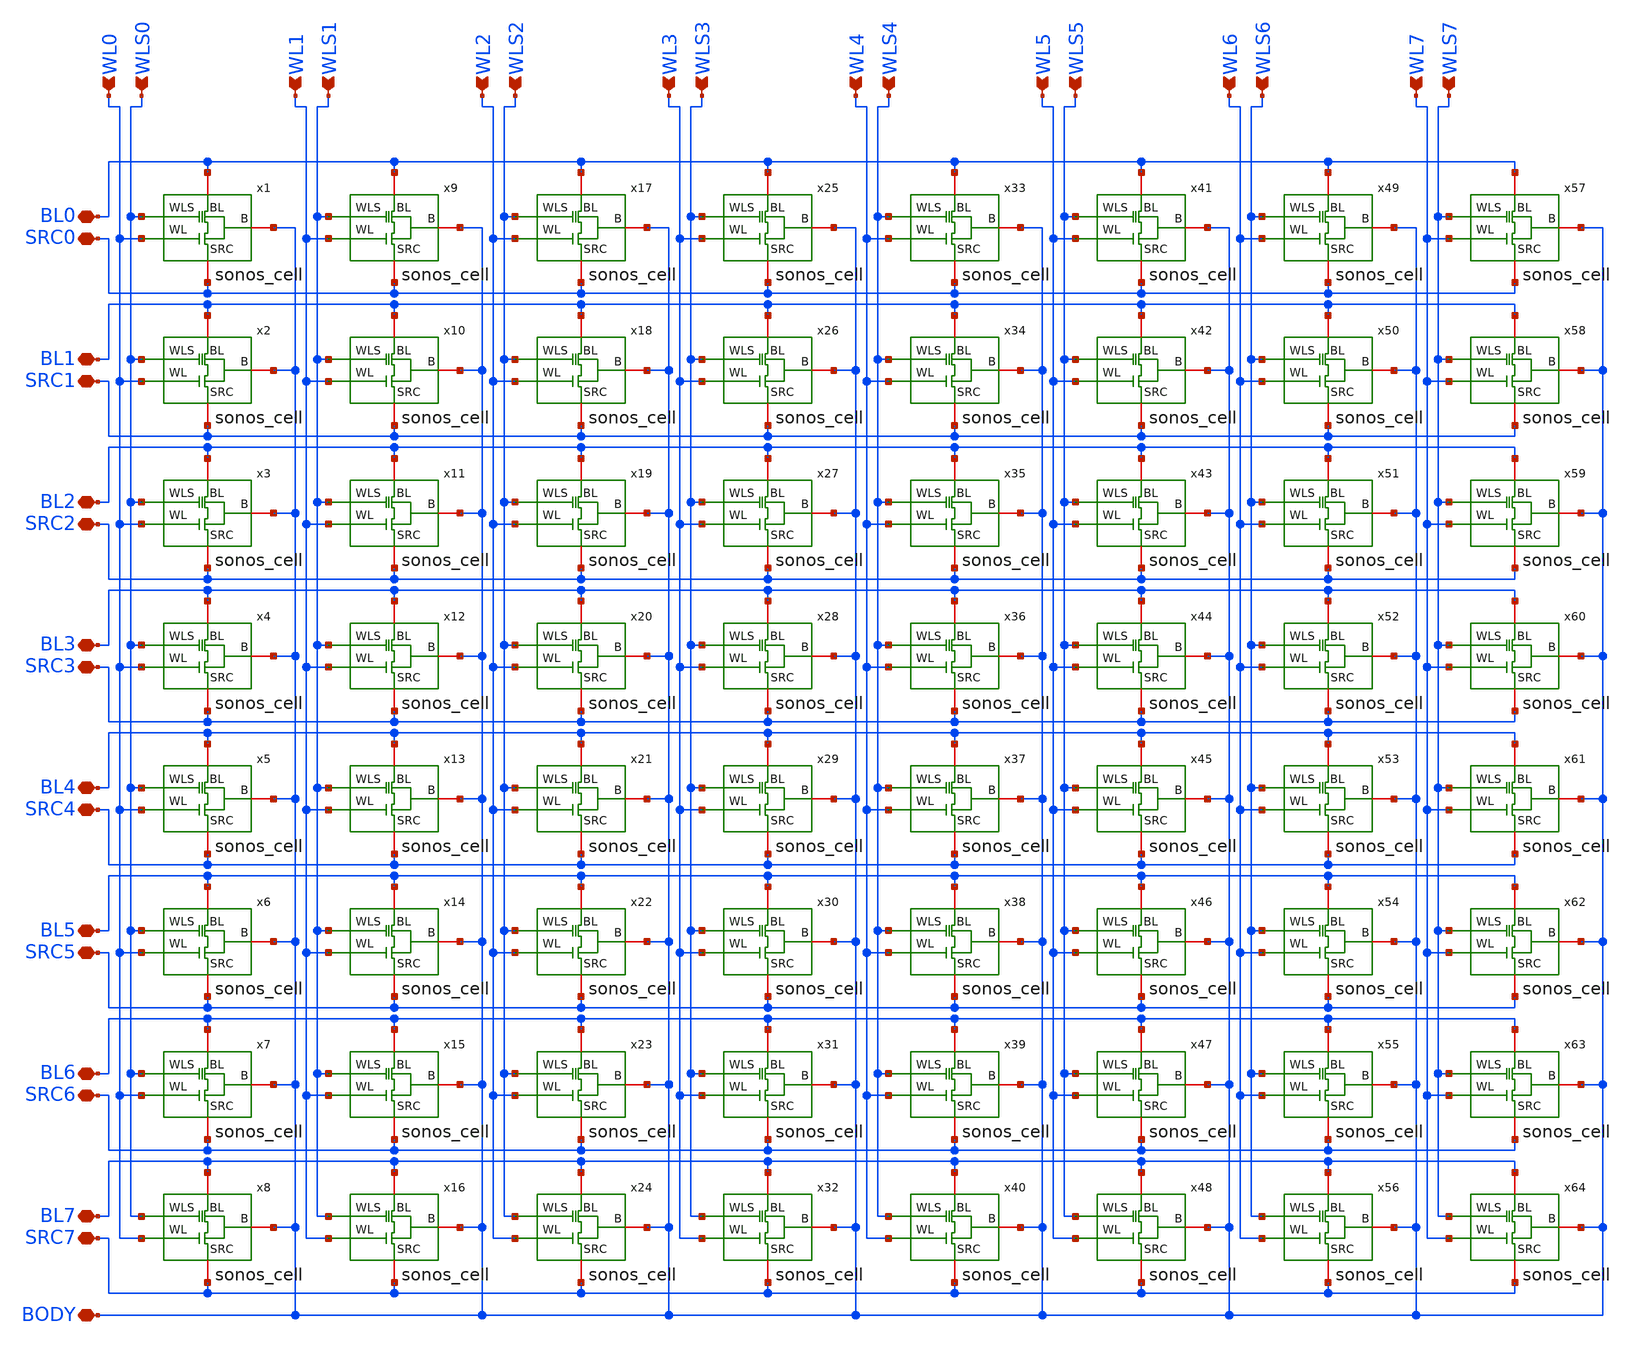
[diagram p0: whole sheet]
** sch_path: xschem/sonos_array.sch
**.subckt sonos_array BL0 WL0 WLS0 WL1 WLS1 WL2 WLS2 WL3 WLS3 WL4 WLS4 WL5 WLS5 WL6 WLS6 WL7 WLS7
*+ BL1 BL2 BL3 BL4 BL5 BL6 BL7 SRC0 SRC1 SRC2 SRC3 SRC4 SRC5 SRC6 SRC7 BODY
*.iopin BL0
*.ipin WL0
*.ipin WLS0
*.ipin WL1
*.ipin WLS1
*.ipin WL2
*.ipin WLS2
*.ipin WL3
*.ipin WLS3
*.ipin WL4
*.ipin WLS4
*.ipin WL5
*.ipin WLS5
*.ipin WL6
*.ipin WLS6
*.ipin WL7
*.ipin WLS7
*.iopin BL1
*.iopin BL2
*.iopin BL3
*.iopin BL4
*.iopin BL5
*.iopin BL6
*.iopin BL7
*.iopin SRC0
*.iopin SRC1
*.iopin SRC2
*.iopin SRC3
*.iopin SRC4
*.iopin SRC5
*.iopin SRC6
*.iopin SRC7
*.iopin BODY
x1 BL0 WLS0 BODY WL0 SRC0 sonos_cell
x2 BL1 WLS0 BODY WL0 SRC1 sonos_cell
x3 BL2 WLS0 BODY WL0 SRC2 sonos_cell
x4 BL3 WLS0 BODY WL0 SRC3 sonos_cell
x5 BL4 WLS0 BODY WL0 SRC4 sonos_cell
x6 BL5 WLS0 BODY WL0 SRC5 sonos_cell
x7 BL6 WLS0 BODY WL0 SRC6 sonos_cell
x8 BL7 WLS0 BODY WL0 SRC7 sonos_cell
x9 BL0 WLS1 BODY WL1 SRC0 sonos_cell
x10 BL1 WLS1 BODY WL1 SRC1 sonos_cell
x11 BL2 WLS1 BODY WL1 SRC2 sonos_cell
x12 BL3 WLS1 BODY WL1 SRC3 sonos_cell
x13 BL4 WLS1 BODY WL1 SRC4 sonos_cell
x14 BL5 WLS1 BODY WL1 SRC5 sonos_cell
x15 BL6 WLS1 BODY WL1 SRC6 sonos_cell
x16 BL7 WLS1 BODY WL1 SRC7 sonos_cell
x17 BL0 WLS2 BODY WL2 SRC0 sonos_cell
x18 BL1 WLS2 BODY WL2 SRC1 sonos_cell
x19 BL2 WLS2 BODY WL2 SRC2 sonos_cell
x20 BL3 WLS2 BODY WL2 SRC3 sonos_cell
x21 BL4 WLS2 BODY WL2 SRC4 sonos_cell
x22 BL5 WLS2 BODY WL2 SRC5 sonos_cell
x23 BL6 WLS2 BODY WL2 SRC6 sonos_cell
x24 BL7 WLS2 BODY WL2 SRC7 sonos_cell
x25 BL0 WLS3 BODY WL3 SRC0 sonos_cell
x26 BL1 WLS3 BODY WL3 SRC1 sonos_cell
x27 BL2 WLS3 BODY WL3 SRC2 sonos_cell
x28 BL3 WLS3 BODY WL3 SRC3 sonos_cell
x29 BL4 WLS3 BODY WL3 SRC4 sonos_cell
x30 BL5 WLS3 BODY WL3 SRC5 sonos_cell
x31 BL6 WLS3 BODY WL3 SRC6 sonos_cell
x32 BL7 WLS3 BODY WL3 SRC7 sonos_cell
x33 BL0 WLS4 BODY WL4 SRC0 sonos_cell
x34 BL1 WLS4 BODY WL4 SRC1 sonos_cell
x35 BL2 WLS4 BODY WL4 SRC2 sonos_cell
x36 BL3 WLS4 BODY WL4 SRC3 sonos_cell
x37 BL4 WLS4 BODY WL4 SRC4 sonos_cell
x38 BL5 WLS4 BODY WL4 SRC5 sonos_cell
x39 BL6 WLS4 BODY WL4 SRC6 sonos_cell
x40 BL7 WLS4 BODY WL4 SRC7 sonos_cell
x41 BL0 WLS5 BODY WL5 SRC0 sonos_cell
x42 BL1 WLS5 BODY WL5 SRC1 sonos_cell
x43 BL2 WLS5 BODY WL5 SRC2 sonos_cell
x44 BL3 WLS5 BODY WL5 SRC3 sonos_cell
x45 BL4 WLS5 BODY WL5 SRC4 sonos_cell
x46 BL5 WLS5 BODY WL5 SRC5 sonos_cell
x47 BL6 WLS5 BODY WL5 SRC6 sonos_cell
x48 BL7 WLS5 BODY WL5 SRC7 sonos_cell
x49 BL0 WLS6 BODY WL6 SRC0 sonos_cell
x50 BL1 WLS6 BODY WL6 SRC1 sonos_cell
x51 BL2 WLS6 BODY WL6 SRC2 sonos_cell
x52 BL3 WLS6 BODY WL6 SRC3 sonos_cell
x53 BL4 WLS6 BODY WL6 SRC4 sonos_cell
x54 BL5 WLS6 BODY WL6 SRC5 sonos_cell
x55 BL6 WLS6 BODY WL6 SRC6 sonos_cell
x56 BL7 WLS6 BODY WL6 SRC7 sonos_cell
x57 BL0 WLS7 BODY WL7 SRC0 sonos_cell
x58 BL1 WLS7 BODY WL7 SRC1 sonos_cell
x59 BL2 WLS7 BODY WL7 SRC2 sonos_cell
x60 BL3 WLS7 BODY WL7 SRC3 sonos_cell
x61 BL4 WLS7 BODY WL7 SRC4 sonos_cell
x62 BL5 WLS7 BODY WL7 SRC5 sonos_cell
x63 BL6 WLS7 BODY WL7 SRC6 sonos_cell
x64 BL7 WLS7 BODY WL7 SRC7 sonos_cell
**.ends

* expanding   symbol:  sonos_cell.sym # of pins=5
** sym_path: xschem/sonos_cell.sym
** sch_path: xschem/sonos_cell.sch
.subckt sonos_cell BL WLS B WL SRC
*.ipin WLS
*.ipin WL
*.iopin B
*.iopin BL
*.iopin SRC
XM1 BL WLS net1 B sky130_fd_bs__special_sonosfet_star L=0.22 W=0.45 m=1
XM2 net1 WL SRC B sky130_fd_bs__special_nfet_pass_flash L=0.15 W=0.45 m=1
.ends

.end
